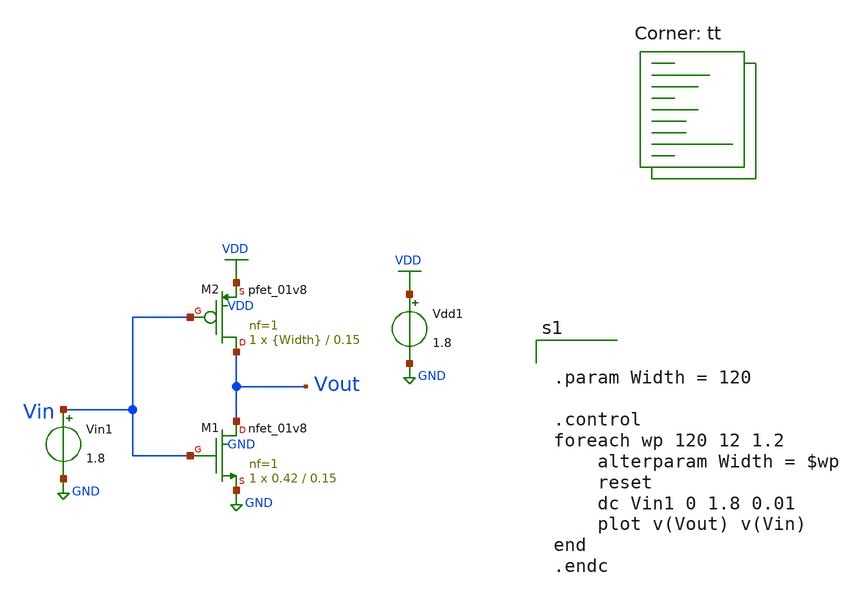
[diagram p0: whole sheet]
** sch_path: Tutorial_2/PMOS_width_vs_VTC.sch
**.subckt PMOS_width_vs_VTC
XM1 Vout Vin GND GND sky130_fd_pr__nfet_01v8 L=0.15 W=0.42 nf=1 ad='int((nf+1)/2) * W/nf * 0.29' as='int((nf+2)/2) * W/nf * 0.29'
+ pd='2*int((nf+1)/2) * (W/nf + 0.29)' ps='2*int((nf+2)/2) * (W/nf + 0.29)' nrd='0.29 / W' nrs='0.29 / W'
+ sa=0 sb=0 sd=0 mult=1 m=1
XM2 Vout Vin VDD VDD sky130_fd_pr__pfet_01v8 L=0.15 W={Width} nf=1 ad='int((nf+1)/2) * W/nf * 0.29' as='int((nf+2)/2) * W/nf * 0.29'
+ pd='2*int((nf+1)/2) * (W/nf + 0.29)' ps='2*int((nf+2)/2) * (W/nf + 0.29)' nrd='0.29 / W' nrs='0.29 / W'
+ sa=0 sb=0 sd=0 mult=1 m=1
Vdd1 VDD GND 1.8
Vin1 Vin GND 1.8
**** begin user architecture code


.param Width = 120

.control
foreach wp 120 12 1.2
	alterparam Width = $wp
	reset
	dc Vin1 0 1.8 0.01
	plot v(Vout) v(Vin)
end
.endc



.lib $::SKYWATER_MODELS/sky130.lib.spice tt
**** end user architecture code
**.ends
.GLOBAL GND
.GLOBAL VDD
.end
